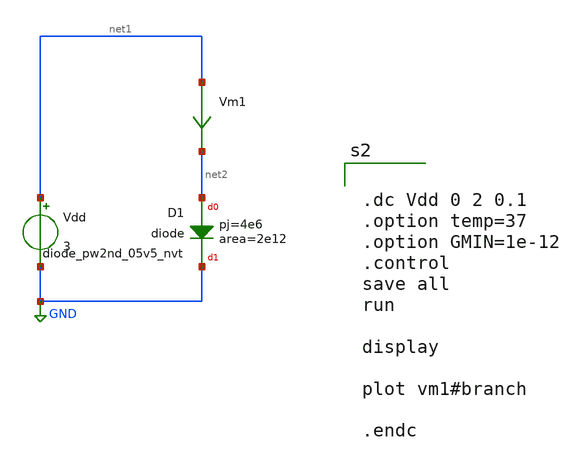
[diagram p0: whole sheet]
** sch_path: xschem/cmos_imager/tb_diode_vi.sch
**.subckt tb_diode_vi
XD1 net2 GND sky130_fd_pr__diode_pw2nd_05v5_nvt area=2e12 pj=4e6
Vdd net1 GND 3
Vm1 net1 net2 0
.save i(vm1)
**** begin user architecture code


.dc Vdd 0 2 0.1
.option temp=37
.option GMIN=1e-12
.control
save all
run

display

plot vm1#branch

.endc



** opencircuitdesign pdks install
.lib $::SKYWATER_MODELS/sky130.lib.spice tt


**** end user architecture code
**.ends
.GLOBAL GND
.end
